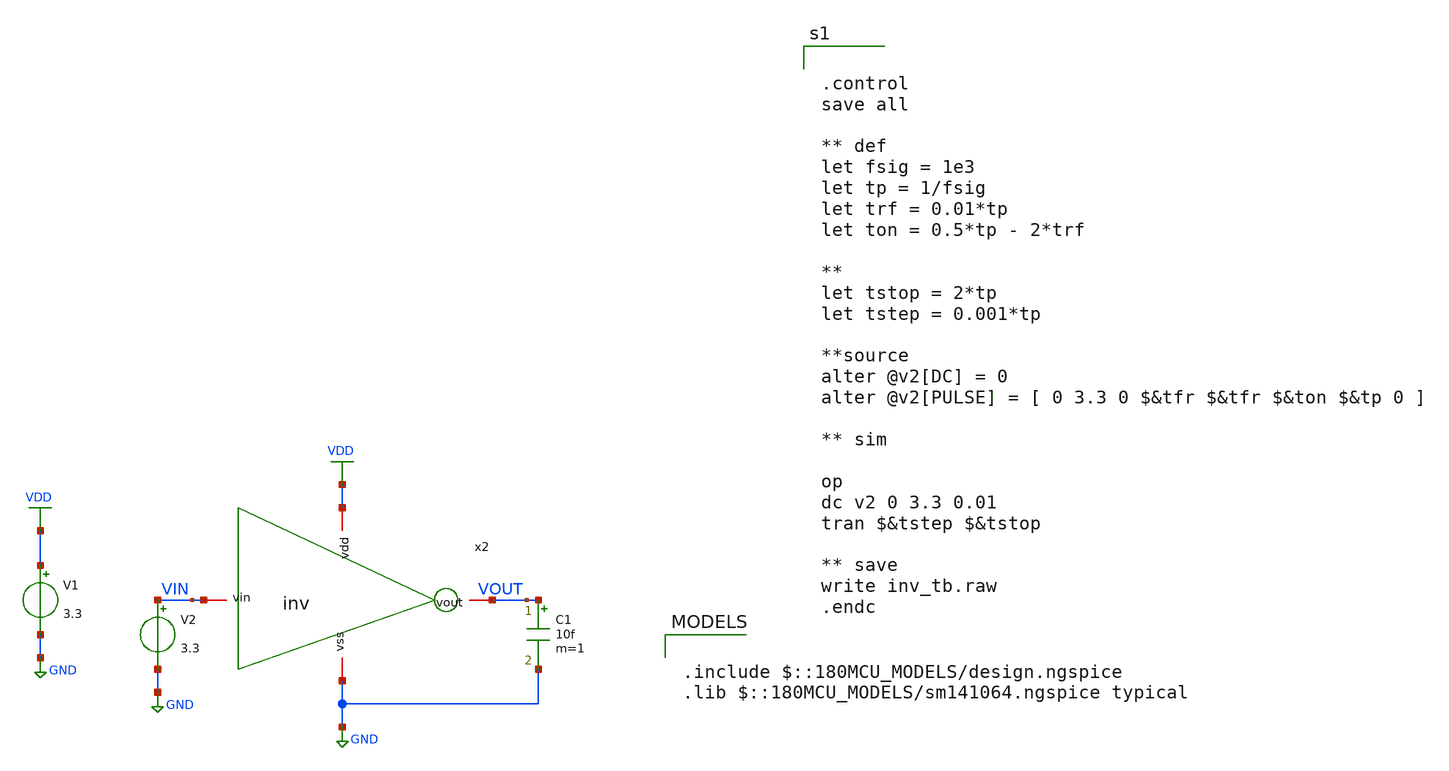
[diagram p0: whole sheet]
** sch_path: src/Pixel/tb.sch
**.subckt tb
V1 VDD GND 3.3
V2 VIN GND 3.3
C1 VOUT GND 10f m=1
x2 VDD VIN VOUT GND inv
**** begin user architecture code

.include $::180MCU_MODELS/design.ngspice
.lib $::180MCU_MODELS/sm141064.ngspice typical



.control
save all

** def
let fsig = 1e3
let tp = 1/fsig
let trf = 0.01*tp
let ton = 0.5*tp - 2*trf

**
let tstop = 2*tp
let tstep = 0.001*tp

**source
alter @v2[DC] = 0
alter @v2[PULSE] = [ 0 3.3 0 $&tfr $&tfr $&ton $&tp 0 ]

** sim

op
dc v2 0 3.3 0.01
tran $&tstep $&tstop

** save
write inv_tb.raw
.endc




**** end user architecture code
**.ends

* expanding   symbol:  pixel/inv.sym # of pins=4
** sym_path: src/Pixel/inv.sym
** sch_path: src/Pixel/inv.sch
.subckt inv vdd vin vout vss
*.iopin vin
*.iopin vout
*.iopin vdd
*.iopin vss
XM1 vout vin vss vss nfet_03v3 L=0.28u W=0.42u nf=1 ad='int((nf+1)/2) * W/nf * 0.18u' as='int((nf+2)/2) * W/nf * 0.18u'
+ pd='2*int((nf+1)/2) * (W/nf + 0.18u)' ps='2*int((nf+2)/2) * (W/nf + 0.18u)' nrd='0.18u / W' nrs='0.18u / W'
+ sa=0 sb=0 sd=0 m=1
XM2 vout vin vdd vdd pfet_03v3 L=0.28u W=0.84u nf=1 ad='int((nf+1)/2) * W/nf * 0.18u' as='int((nf+2)/2) * W/nf * 0.18u'
+ pd='2*int((nf+1)/2) * (W/nf + 0.18u)' ps='2*int((nf+2)/2) * (W/nf + 0.18u)' nrd='0.18u / W' nrs='0.18u / W'
+ sa=0 sb=0 sd=0 m=1
.ends

.GLOBAL VDD
.GLOBAL GND
.end
